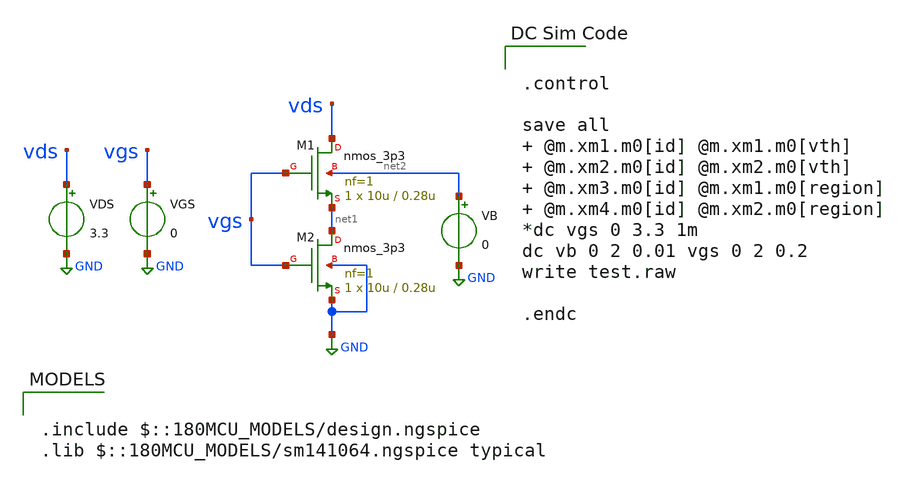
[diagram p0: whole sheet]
** sch_path: Tinkering/test.sch
**.subckt test
XM1 vds vgs net1 net2 nmos_3p3 L=0.28u W=10u nf=1 ad='int((nf+1)/2) * W/nf * 0.18u' as='int((nf+2)/2) * W/nf * 0.18u'
+ pd='2*int((nf+1)/2) * (W/nf + 0.18u)' ps='2*int((nf+2)/2) * (W/nf + 0.18u)' nrd='0.18u / W' nrs='0.18u / W'
+ sa=0 sb=0 sd=0 m=1
XM2 net1 vgs GND GND nmos_3p3 L=0.28u W=10u nf=1 ad='int((nf+1)/2) * W/nf * 0.18u' as='int((nf+2)/2) * W/nf * 0.18u'
+ pd='2*int((nf+1)/2) * (W/nf + 0.18u)' ps='2*int((nf+2)/2) * (W/nf + 0.18u)' nrd='0.18u / W' nrs='0.18u / W'
+ sa=0 sb=0 sd=0 m=1
VDS vds GND 3.3
VGS vgs GND 0
VB net2 GND 0
**** begin user architecture code

.include $::180MCU_MODELS/design.ngspice
.lib $::180MCU_MODELS/sm141064.ngspice typical



.control

save all   @m.xm1.m0[id] @m.xm1.m0[vth]  @m.xm2.m0[id] @m.xm2.m0[vth]  @m.xm3.m0[id]
+ @m.xm1.m0[region]  @m.xm4.m0[id] @m.xm2.m0[region]
*dc vgs 0 3.3 1m
dc vb 0 2 0.01 vgs 0 2 0.2
write test.raw

.endc


**** end user architecture code
**.ends
.GLOBAL GND
.end
